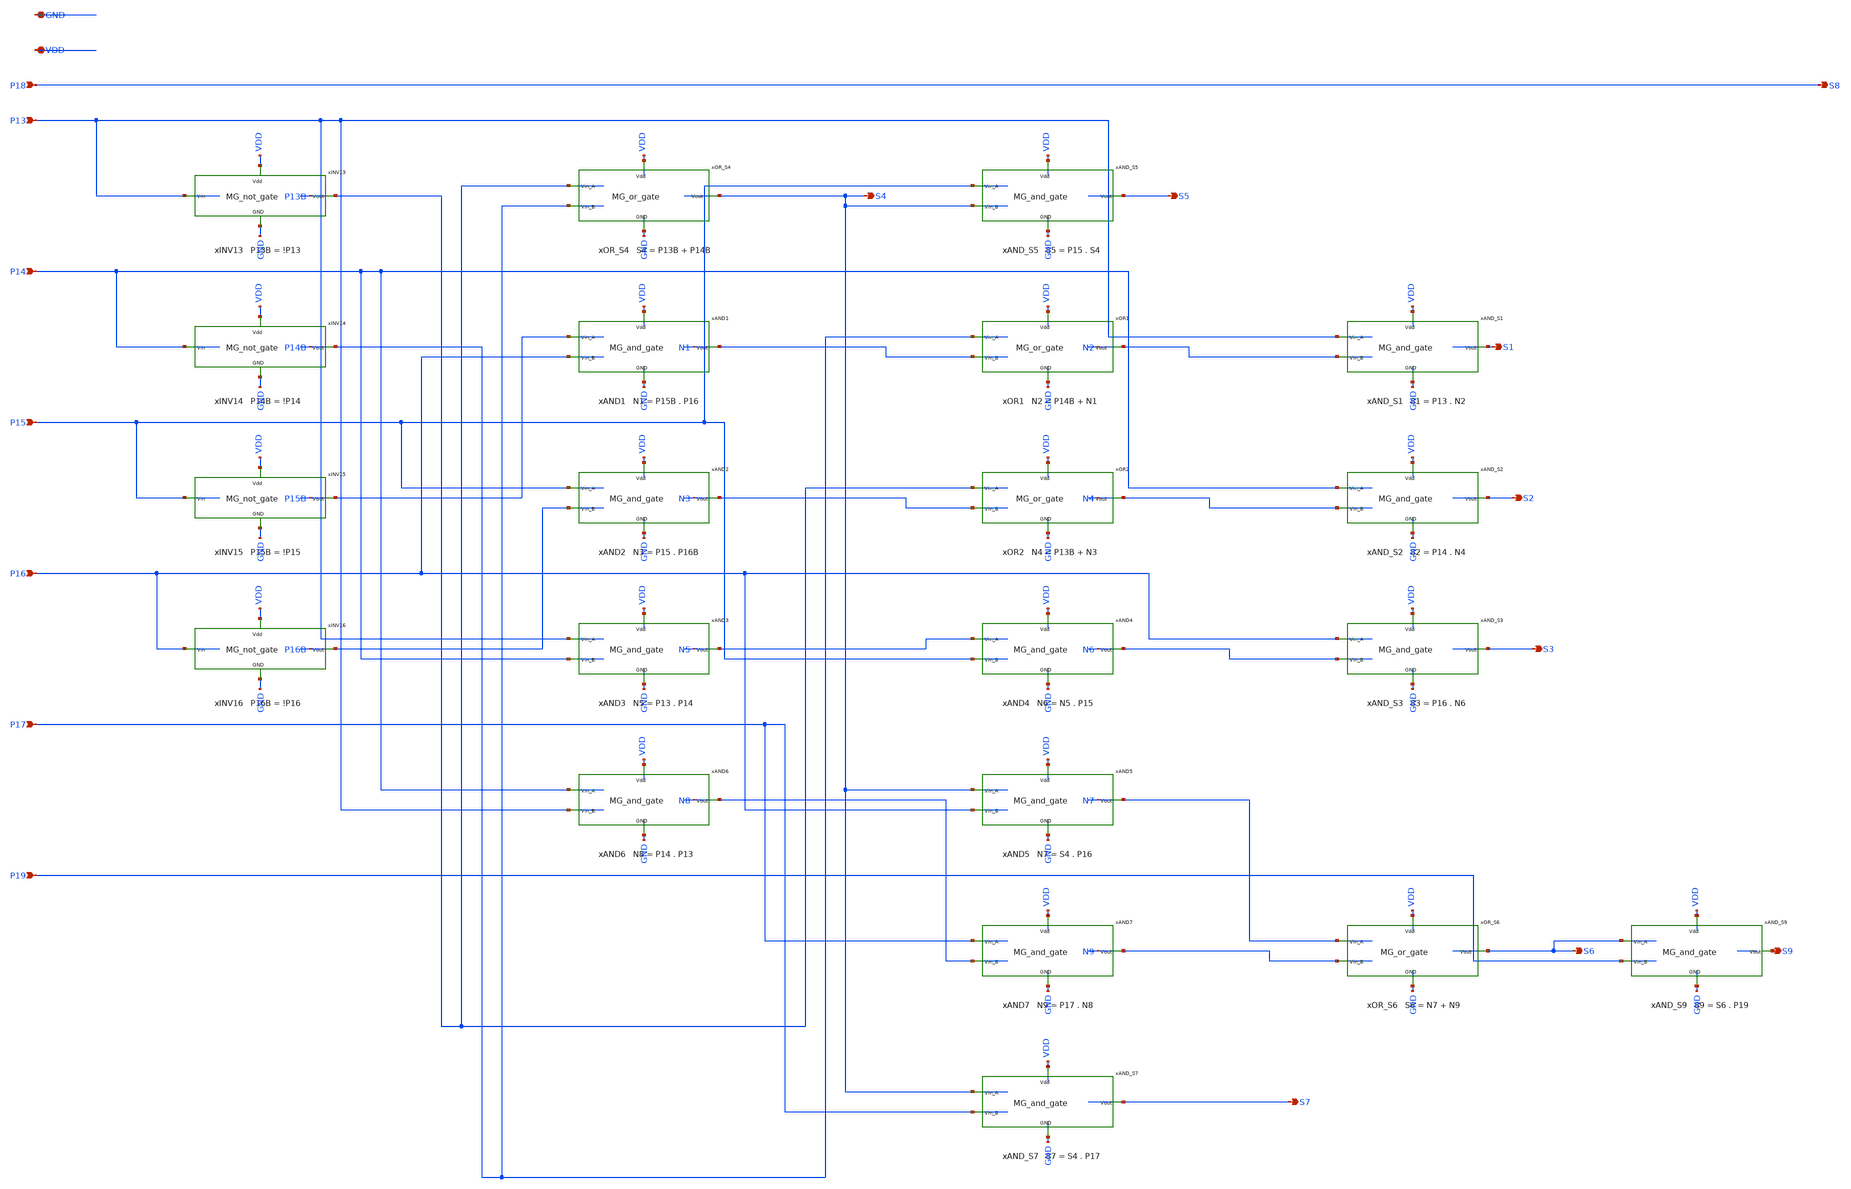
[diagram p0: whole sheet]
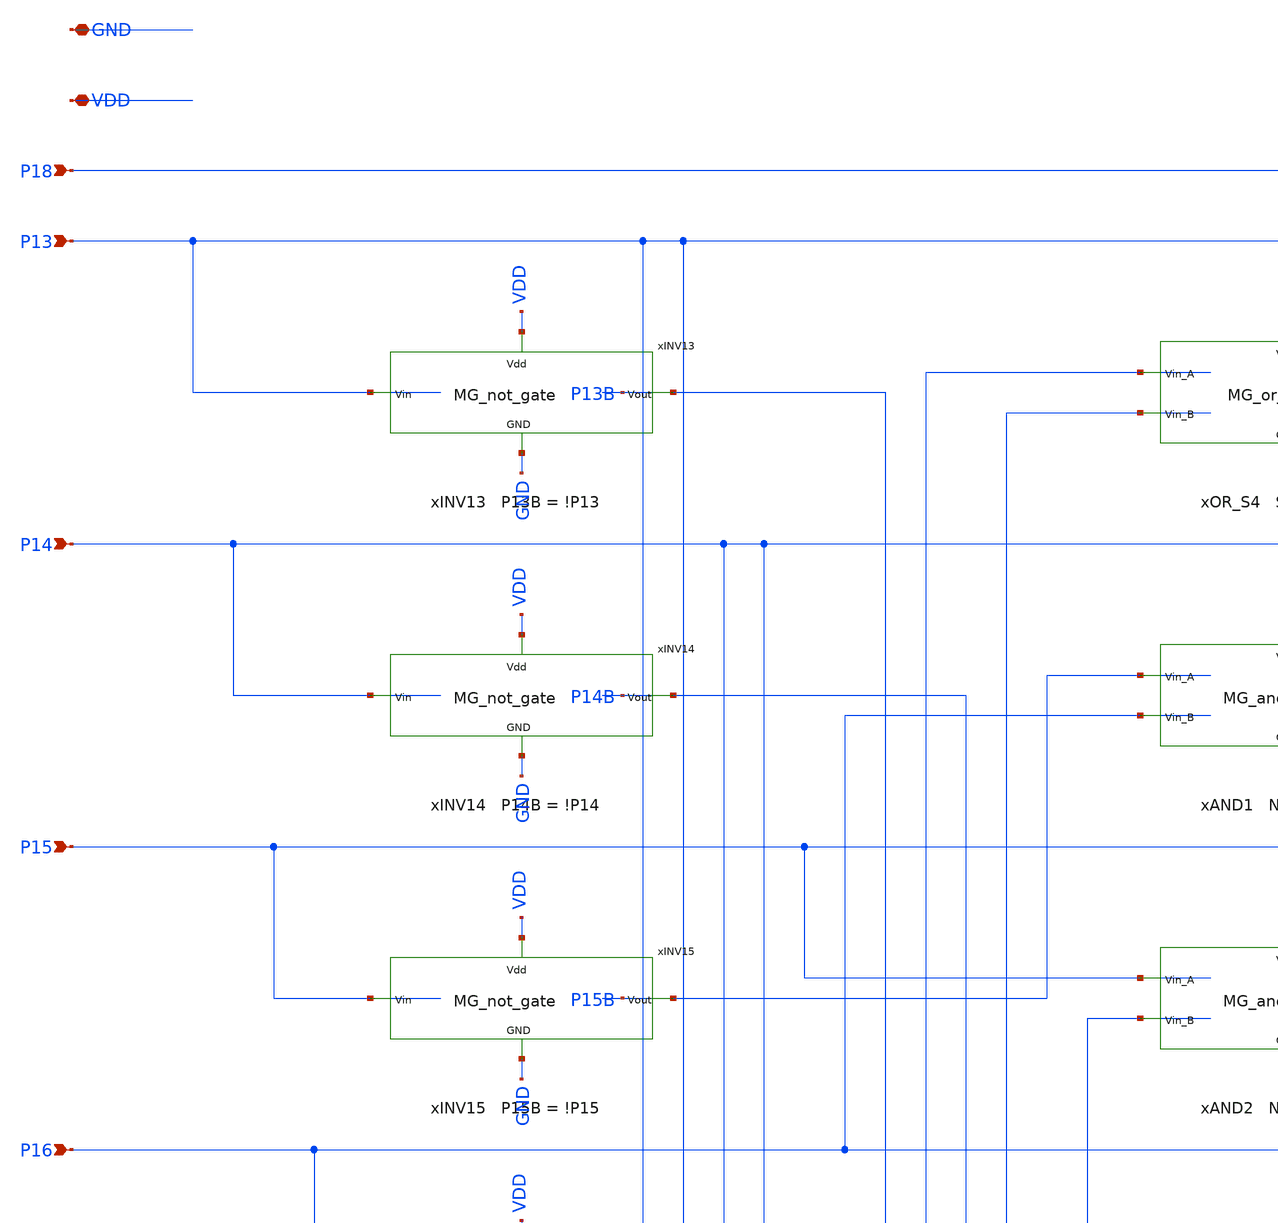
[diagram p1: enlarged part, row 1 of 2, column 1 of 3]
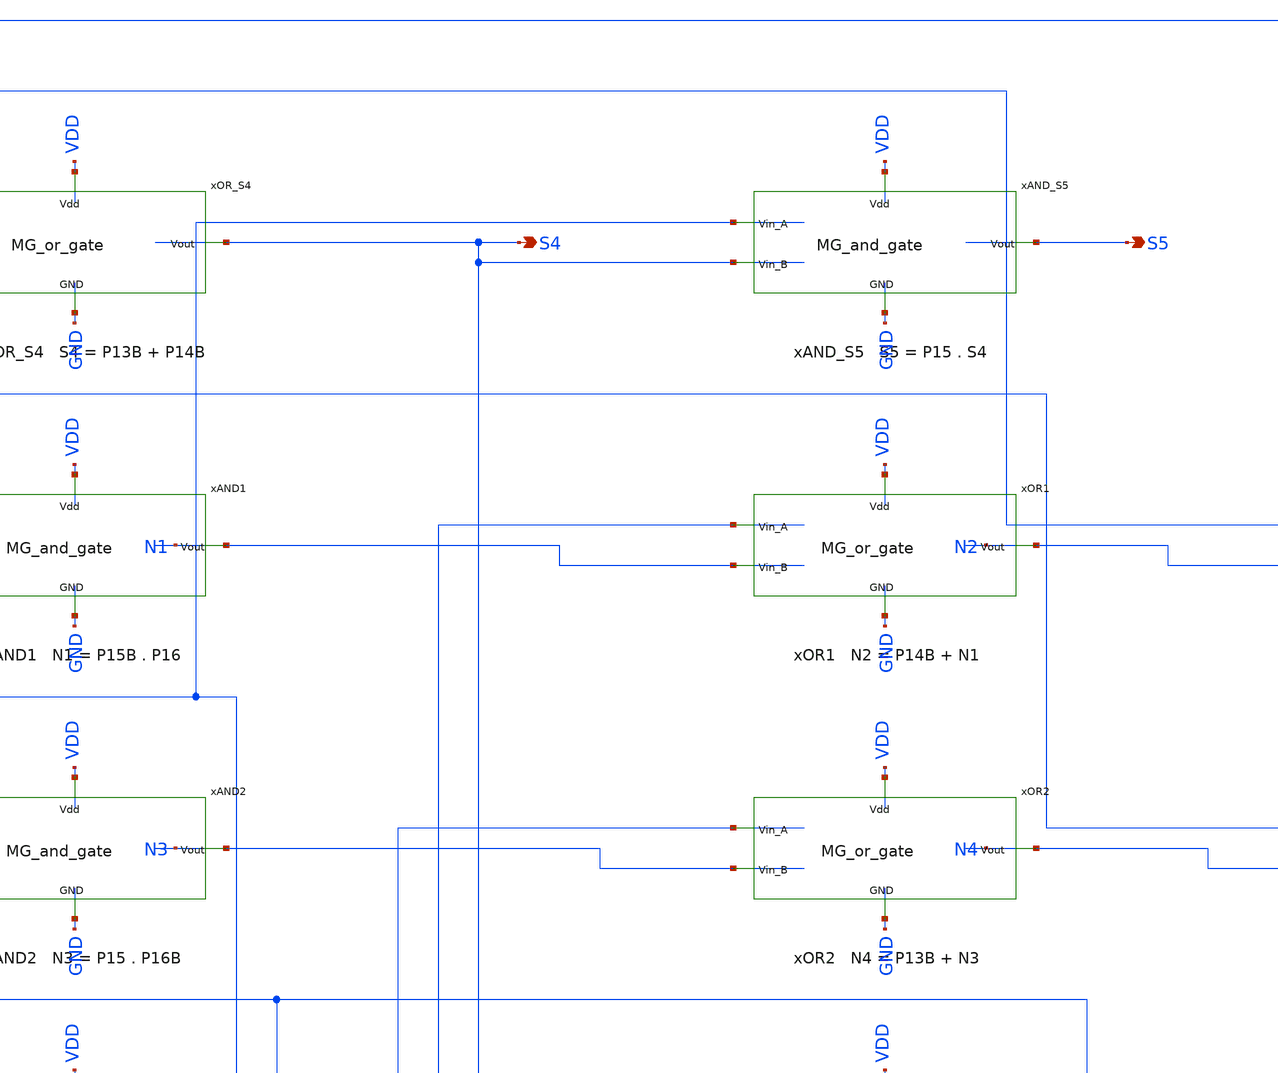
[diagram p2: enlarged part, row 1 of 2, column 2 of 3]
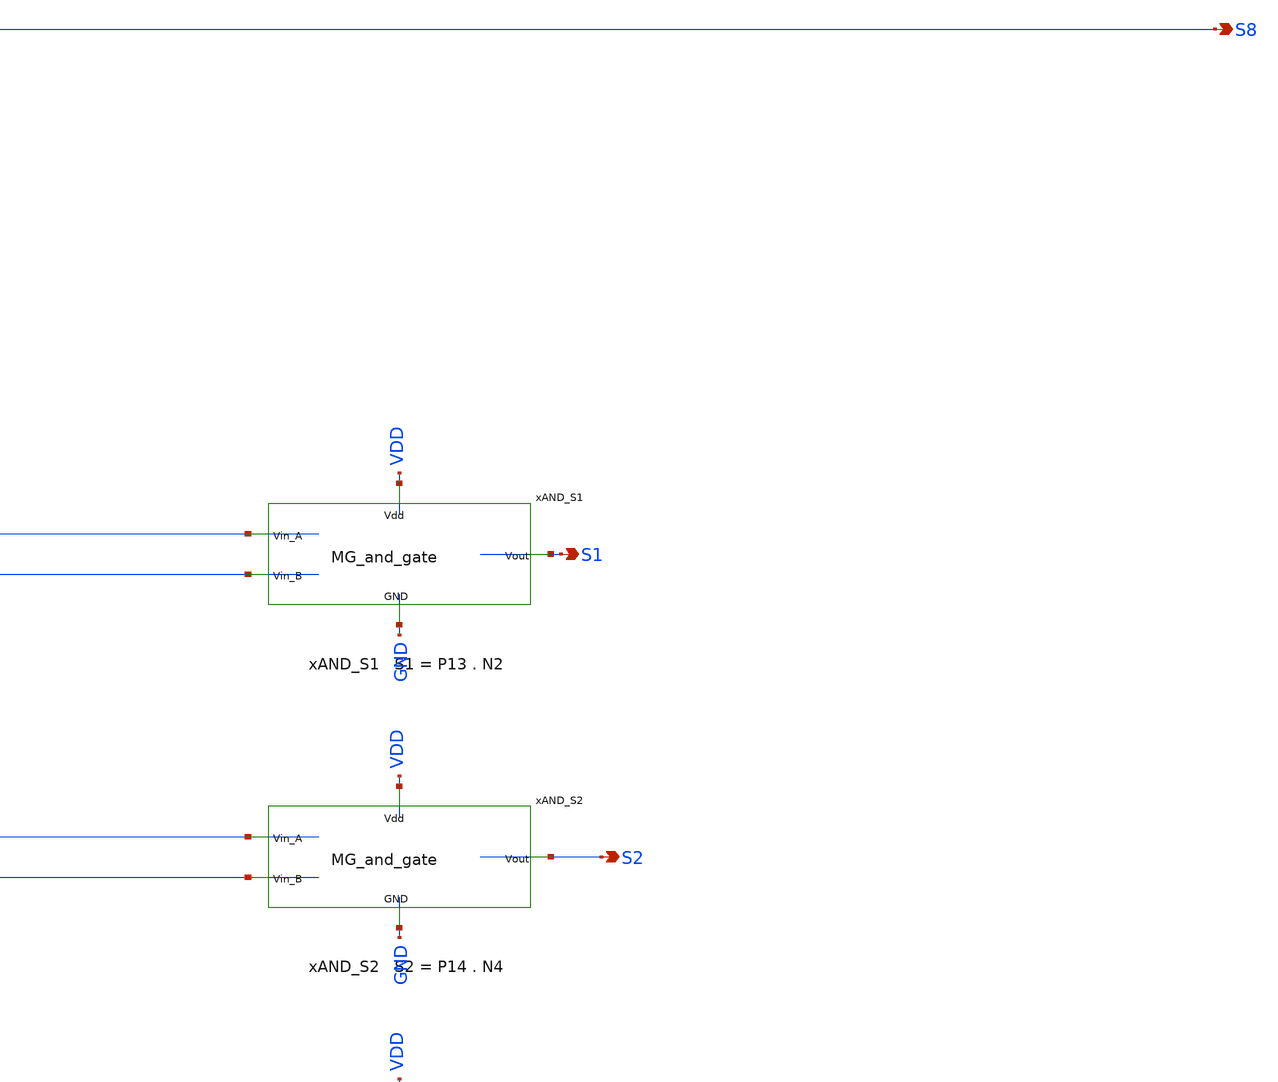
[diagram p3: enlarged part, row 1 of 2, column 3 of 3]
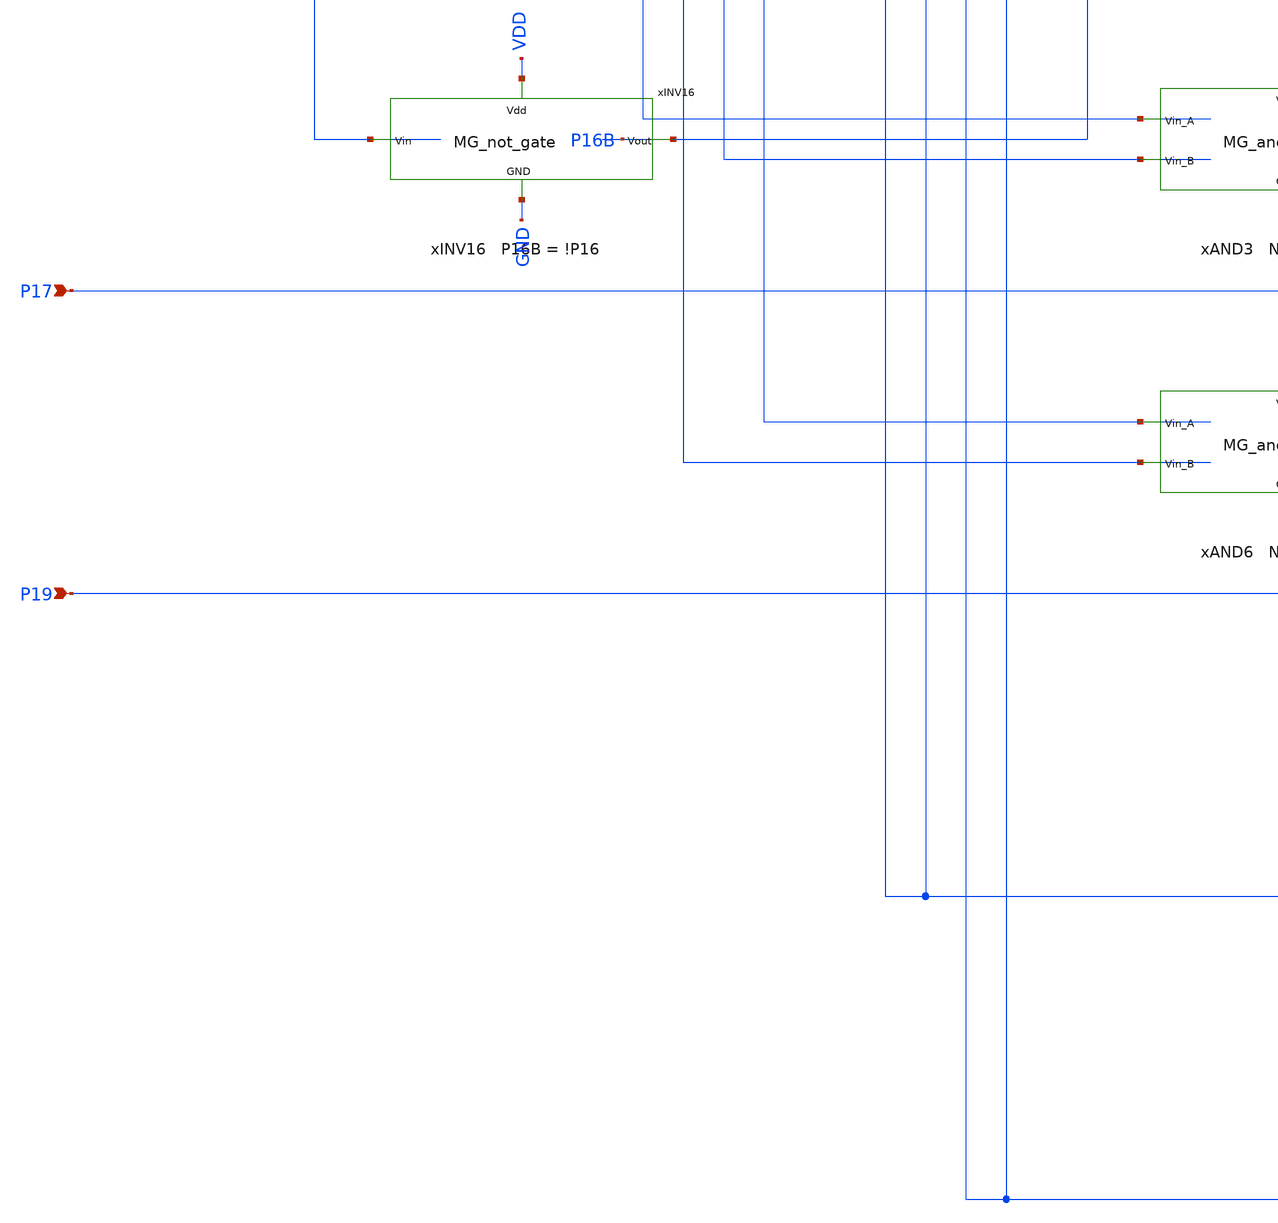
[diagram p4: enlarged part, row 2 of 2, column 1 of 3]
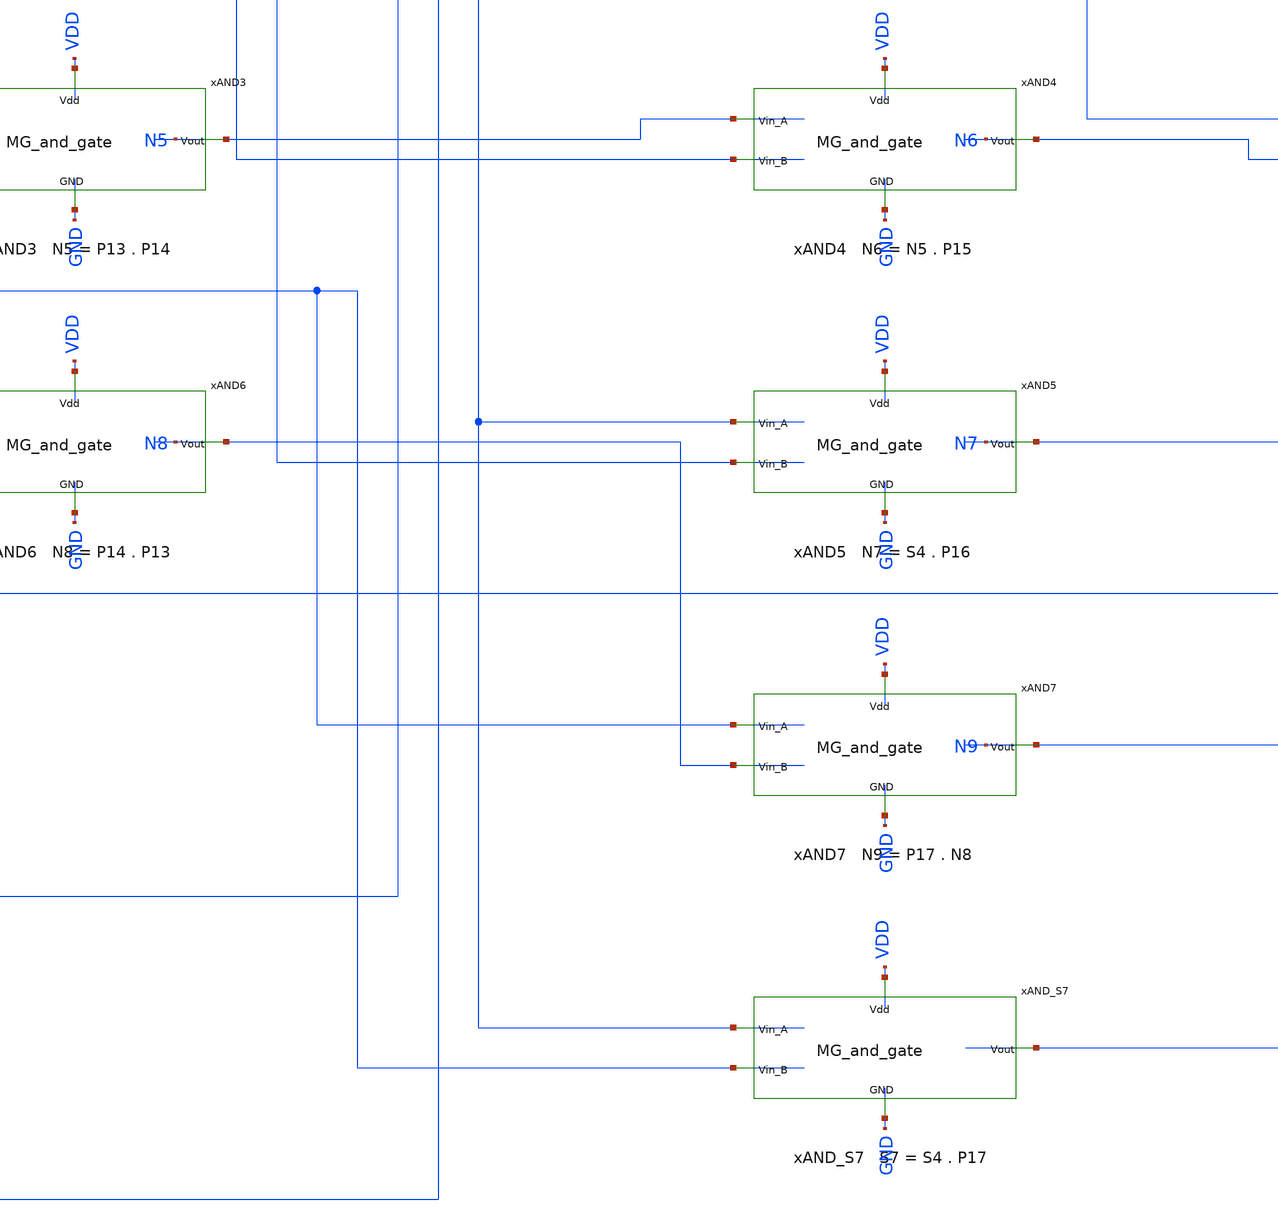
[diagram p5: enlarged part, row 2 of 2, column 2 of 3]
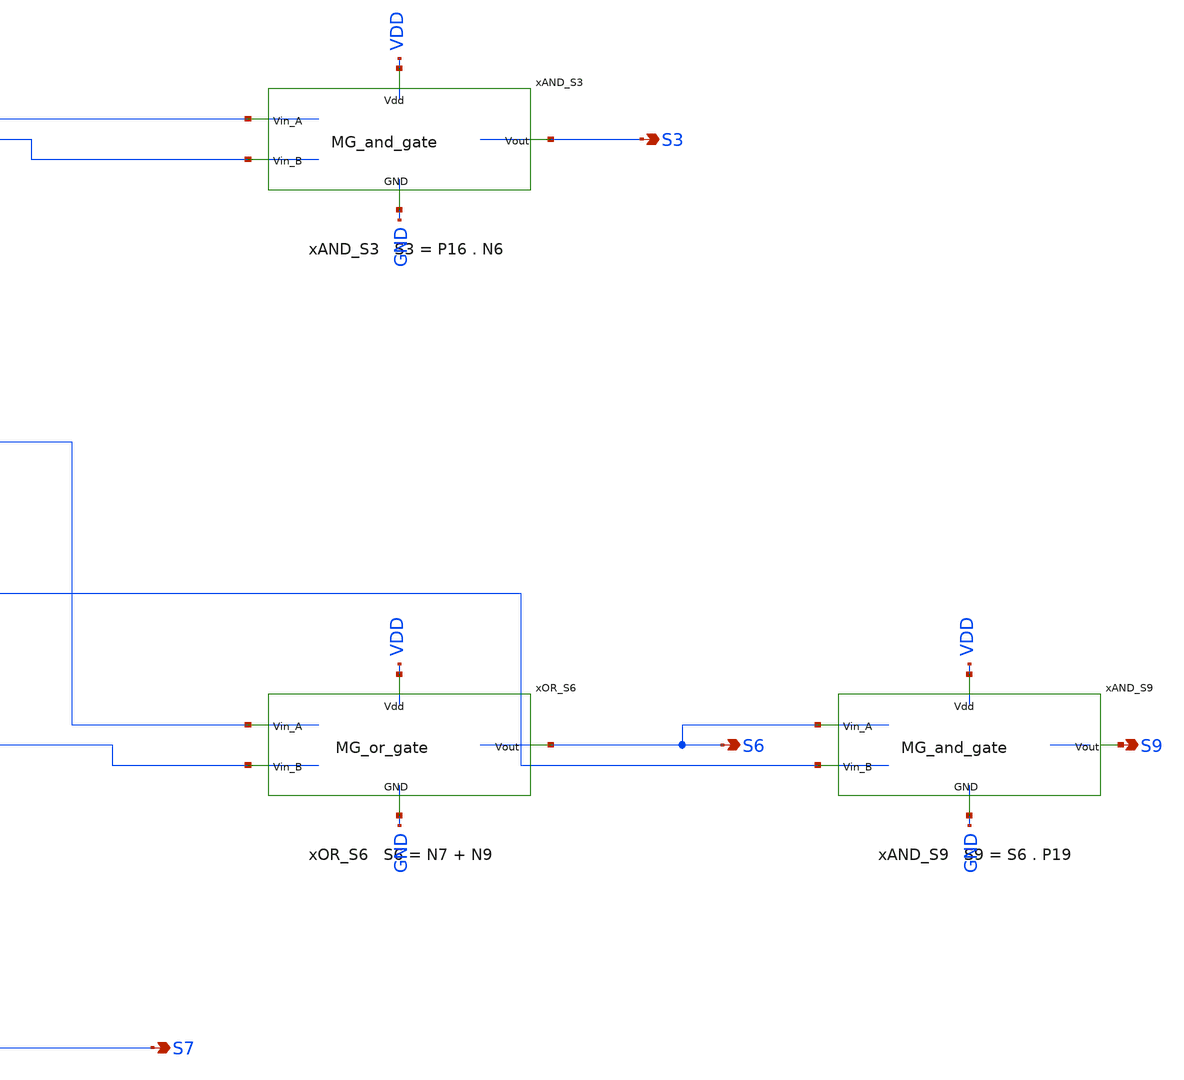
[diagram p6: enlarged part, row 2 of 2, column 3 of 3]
** sch_path: MG_decoder/decoder_routed.sch
**.subckt decoder_routed P13 P14 P15 P16 P17 P19 P18 S8 VDD GND S4 S5 S7 S1 S2 S3 S6 S9
*.ipin P13
*.ipin P14
*.ipin P15
*.ipin P16
*.ipin P17
*.ipin P19
*.ipin P18
*.opin S8
*.iopin VDD
*.iopin GND
*.opin S4
*.opin S5
*.opin S7
*.opin S1
*.opin S2
*.opin S3
*.opin S6
*.opin S9
xINV13 VDD P13 P13B GND MG_not_gate
xINV14 VDD P14 P14B GND MG_not_gate
xINV15 VDD P15 P15B GND MG_not_gate
xINV16 VDD P16 P16B GND MG_not_gate
xOR_S4 VDD P13B S4 P14B GND MG_or_gate
xAND1 VDD P15B P16 N1 GND MG_and_gate
xAND2 VDD P15 P16B N3 GND MG_and_gate
xAND3 VDD P13 P14 N5 GND MG_and_gate
xAND6 VDD P14 P13 N8 GND MG_and_gate
xAND_S5 VDD P15 S4 S5 GND MG_and_gate
xOR1 VDD P14B N2 N1 GND MG_or_gate
xOR2 VDD P13B N4 N3 GND MG_or_gate
xAND4 VDD N5 P15 N6 GND MG_and_gate
xAND5 VDD S4 P16 N7 GND MG_and_gate
xAND7 VDD P17 N8 N9 GND MG_and_gate
xAND_S7 VDD S4 P17 S7 GND MG_and_gate
xAND_S1 VDD P13 N2 S1 GND MG_and_gate
xAND_S2 VDD P14 N4 S2 GND MG_and_gate
xAND_S3 VDD P16 N6 S3 GND MG_and_gate
xOR_S6 VDD N7 S6 N9 GND MG_or_gate
xAND_S9 VDD S6 P19 S9 GND MG_and_gate
**.ends

* expanding   symbol:  MG_not_gate.sym # of pins=4
** sym_path: MG_decoder/MG_not_gate.sym
** sch_path: MG_decoder/MG_not_gate.sch
.subckt MG_not_gate Vdd Vin Vout GND
*.ipin Vdd
*.ipin GND
*.ipin Vin
*.ipin Vout
XM1 Vout Vin Vdd Vdd pfet_05v0 L=0.6u W=2.2u nf=2 ad='int((nf+1)/2) * W/nf * 0.18u' as='int((nf+2)/2) * W/nf * 0.18u'
+ pd='2*int((nf+1)/2) * (W/nf + 0.18u)' ps='2*int((nf+2)/2) * (W/nf + 0.18u)' nrd='0.18u / W' nrs='0.18u / W'
+ sa=0 sb=0 sd=0 m=1
XM2 Vout Vin GND GND nfet_05v0 L=0.6u W=1u nf=1 ad='int((nf+1)/2) * W/nf * 0.18u' as='int((nf+2)/2) * W/nf * 0.18u'
+ pd='2*int((nf+1)/2) * (W/nf + 0.18u)' ps='2*int((nf+2)/2) * (W/nf + 0.18u)' nrd='0.18u / W' nrs='0.18u / W'
+ sa=0 sb=0 sd=0 m=1
.ends


* expanding   symbol:  MG_or_gate.sym # of pins=5
** sym_path: MG_decoder/MG_or_gate.sym
** sch_path: MG_decoder/MG_or_gate.sch
.subckt MG_or_gate Vdd Vin_A Vout Vin_B GND
*.ipin Vdd
*.ipin GND
*.ipin Vin_A
*.ipin Vout
*.ipin Vin_B
XM1 Vout net1 Vdd Vdd pfet_05v0 L=0.6u W=2.2u nf=2 ad='int((nf+1)/2) * W/nf * 0.18u' as='int((nf+2)/2) * W/nf * 0.18u'
+ pd='2*int((nf+1)/2) * (W/nf + 0.18u)' ps='2*int((nf+2)/2) * (W/nf + 0.18u)' nrd='0.18u / W' nrs='0.18u / W'
+ sa=0 sb=0 sd=0 m=1
XM2 Vout net1 GND GND nfet_05v0 L=0.6u W=1u nf=1 ad='int((nf+1)/2) * W/nf * 0.18u' as='int((nf+2)/2) * W/nf * 0.18u'
+ pd='2*int((nf+1)/2) * (W/nf + 0.18u)' ps='2*int((nf+2)/2) * (W/nf + 0.18u)' nrd='0.18u / W' nrs='0.18u / W'
+ sa=0 sb=0 sd=0 m=1
XM3 net1 Vin_B net2 Vdd pfet_05v0 L=0.6u W=2.2u nf=2 ad='int((nf+1)/2) * W/nf * 0.18u' as='int((nf+2)/2) * W/nf * 0.18u'
+ pd='2*int((nf+1)/2) * (W/nf + 0.18u)' ps='2*int((nf+2)/2) * (W/nf + 0.18u)' nrd='0.18u / W' nrs='0.18u / W'
+ sa=0 sb=0 sd=0 m=1
XM4 net2 Vin_A Vdd Vdd pfet_05v0 L=0.6u W=2.2u nf=2 ad='int((nf+1)/2) * W/nf * 0.18u' as='int((nf+2)/2) * W/nf * 0.18u'
+ pd='2*int((nf+1)/2) * (W/nf + 0.18u)' ps='2*int((nf+2)/2) * (W/nf + 0.18u)' nrd='0.18u / W' nrs='0.18u / W'
+ sa=0 sb=0 sd=0 m=1
XM5 net1 Vin_A GND GND nfet_05v0 L=0.6u W=2u nf=1 ad='int((nf+1)/2) * W/nf * 0.18u' as='int((nf+2)/2) * W/nf * 0.18u'
+ pd='2*int((nf+1)/2) * (W/nf + 0.18u)' ps='2*int((nf+2)/2) * (W/nf + 0.18u)' nrd='0.18u / W' nrs='0.18u / W'
+ sa=0 sb=0 sd=0 m=1
XM6 net1 Vin_B GND GND nfet_05v0 L=0.6u W=2u nf=1 ad='int((nf+1)/2) * W/nf * 0.18u' as='int((nf+2)/2) * W/nf * 0.18u'
+ pd='2*int((nf+1)/2) * (W/nf + 0.18u)' ps='2*int((nf+2)/2) * (W/nf + 0.18u)' nrd='0.18u / W' nrs='0.18u / W'
+ sa=0 sb=0 sd=0 m=1
.ends


* expanding   symbol:  MG_and_gate.sym # of pins=5
** sym_path: MG_decoder/MG_and_gate.sym
** sch_path: MG_decoder/MG_and_gate.sch
.subckt MG_and_gate Vdd Vin_A Vin_B Vout GND
*.ipin Vdd
*.ipin GND
*.ipin Vin_A
*.opin Vout
*.ipin Vin_B
XM1 Vout net1 Vdd Vdd pfet_05v0 L=0.7u W=2.2u nf=2 ad='int((nf+1)/2) * W/nf * 0.18u' as='int((nf+2)/2) * W/nf * 0.18u'
+ pd='2*int((nf+1)/2) * (W/nf + 0.18u)' ps='2*int((nf+2)/2) * (W/nf + 0.18u)' nrd='0.18u / W' nrs='0.18u / W'
+ sa=0 sb=0 sd=0 m=1
XM2 Vout net1 GND GND nfet_05v0 L=0.7u W=1u nf=1 ad='int((nf+1)/2) * W/nf * 0.18u' as='int((nf+2)/2) * W/nf * 0.18u'
+ pd='2*int((nf+1)/2) * (W/nf + 0.18u)' ps='2*int((nf+2)/2) * (W/nf + 0.18u)' nrd='0.18u / W' nrs='0.18u / W'
+ sa=0 sb=0 sd=0 m=1
XM3 net1 Vin_A Vdd Vdd pfet_05v0 L=0.7u W=2.2u nf=2 ad='int((nf+1)/2) * W/nf * 0.18u' as='int((nf+2)/2) * W/nf * 0.18u'
+ pd='2*int((nf+1)/2) * (W/nf + 0.18u)' ps='2*int((nf+2)/2) * (W/nf + 0.18u)' nrd='0.18u / W' nrs='0.18u / W'
+ sa=0 sb=0 sd=0 m=1
XM4 net1 Vin_B Vdd Vdd pfet_05v0 L=0.7u W=2.2u nf=2 ad='int((nf+1)/2) * W/nf * 0.18u' as='int((nf+2)/2) * W/nf * 0.18u'
+ pd='2*int((nf+1)/2) * (W/nf + 0.18u)' ps='2*int((nf+2)/2) * (W/nf + 0.18u)' nrd='0.18u / W' nrs='0.18u / W'
+ sa=0 sb=0 sd=0 m=1
XM5 net1 Vin_A net2 GND nfet_05v0 L=0.7u W=2u nf=1 ad='int((nf+1)/2) * W/nf * 0.18u' as='int((nf+2)/2) * W/nf * 0.18u'
+ pd='2*int((nf+1)/2) * (W/nf + 0.18u)' ps='2*int((nf+2)/2) * (W/nf + 0.18u)' nrd='0.18u / W' nrs='0.18u / W'
+ sa=0 sb=0 sd=0 m=1
XM6 net2 Vin_B GND GND nfet_05v0 L=0.7u W=2u nf=1 ad='int((nf+1)/2) * W/nf * 0.18u' as='int((nf+2)/2) * W/nf * 0.18u'
+ pd='2*int((nf+1)/2) * (W/nf + 0.18u)' ps='2*int((nf+2)/2) * (W/nf + 0.18u)' nrd='0.18u / W' nrs='0.18u / W'
+ sa=0 sb=0 sd=0 m=1
XC1 Vdd GND cap_nmos_06v0 c_width=30e-6 c_length=30e-6 m=1
.ends

.end
